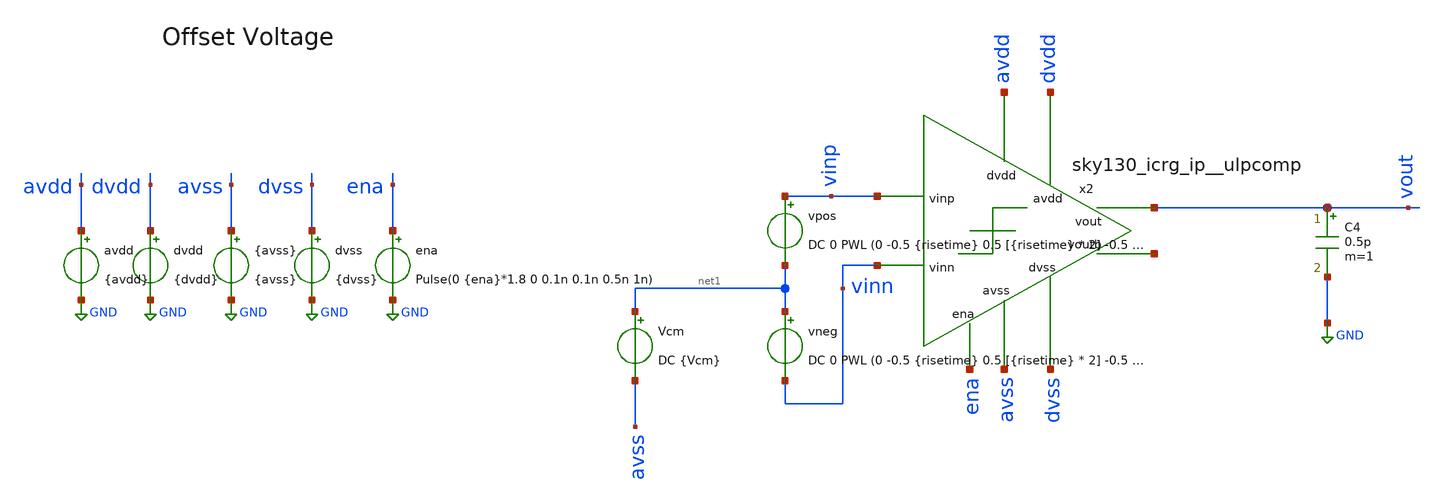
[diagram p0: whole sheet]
** sch_path: cace/tb_offset_voltage.sch
**.subckt tb_offset_voltage
x2 avdd dvdd ena vinp vinn vout net2 avss dvss sky130_icrg_ip__ulpcomp
vpos vinp net1 DC 0 PWL (0 -0.5 {risetime} 0.5 [{risetime} * 2] -0.5 [{risetime} * 3] 0.5 [{risetime}
+ * 4] -0.5 )
avdd avdd GND {avdd}
dvdd dvdd GND {dvdd}
{avss} avss GND {avss}
dvss dvss GND {dvss}
C4 vout GND 0.5p m=1
Vcm net1 avss DC {Vcm}
ena ena GND Pulse(0 {ena}*1.8 0 0.1n 0.1n 0.5n 1n)
vneg net1 vinn DC 0 PWL (0 -0.5 {risetime} 0.5 [{risetime} * 2] -0.5 [{risetime} * 3] 0.5 [{risetime}
+ * 4] -0.5 )
**** begin user architecture code


.lib /home/ttuser/pdk/sky130A/libs.tech/combined/sky130.lib.spice {corner}
.option TEMP={temperature}


.control
** Find zero crossing for positive input differential, zero crossing for negative
** input differential, then compute the average
tran [{risetime} * 2 / 1000] [{risetime} * 2]
meas tran vhigh FIND V(vinp) WHEN V(vout) = [{dvdd} / 2] CROSS=1
meas tran vlow FIND V(vinp) WHEN V(vout) = [{dvdd} / 2] CROSS=2
let vrise = $&vhigh - {Vcm}
let vfall = $&vlow - {Vcm}

let voffset = 0.5 * ($&vrise + $&vfall)
let vhyst = $&vrise - $&vfall

echo $&voffset $&vhyst > {simpath}/{filename}_{N}.data
*set wr_singlescale
*wrdata {simpath}/{filename}_{N}.data V(out) V(inp) V(inm)
quit
.endc


**** end user architecture code
**.ends
.GLOBAL GND
.end
